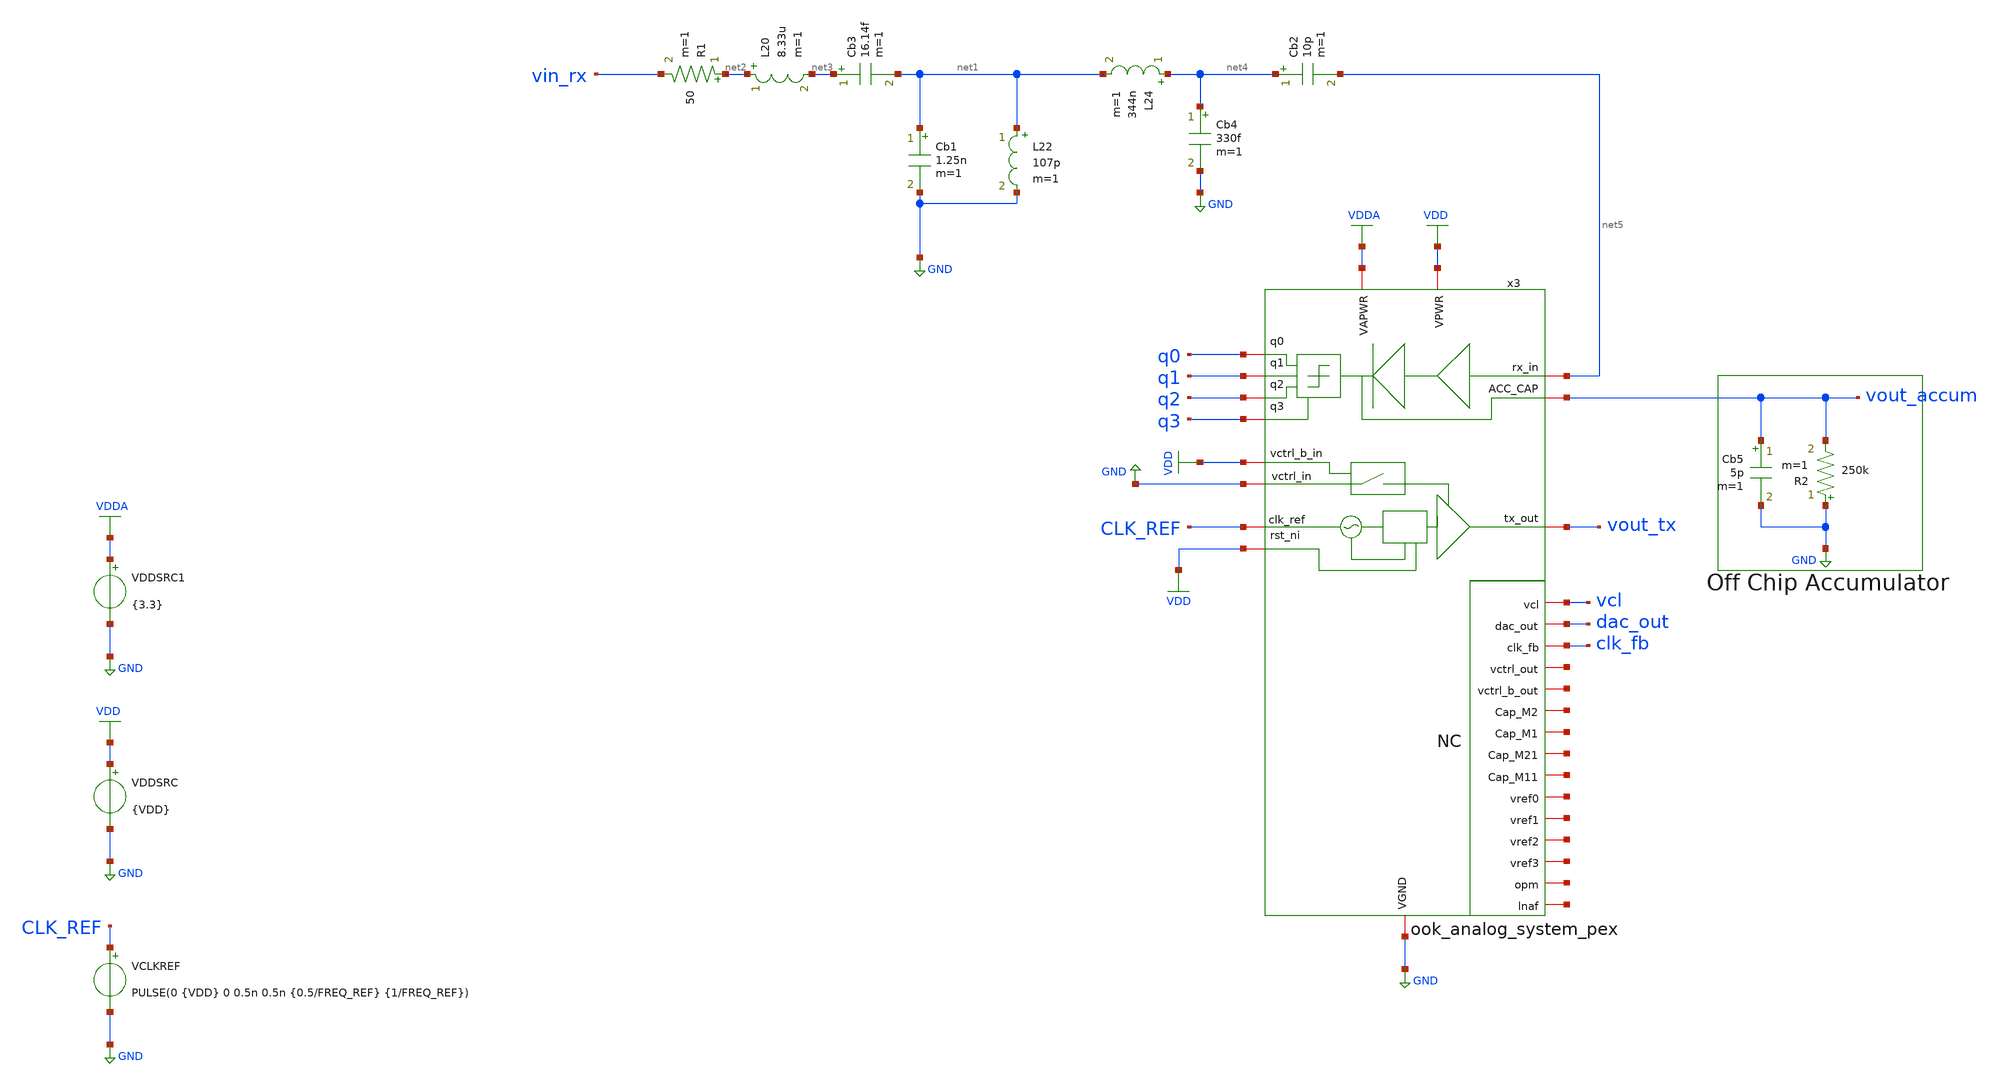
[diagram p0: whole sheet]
** sch_path: macros/heichips26_ook_top/macros/ook_analog_system/testbenches/xschem/ook_analog_system_tb_tran.sch
**.subckt ook_analog_system_tb_tran
VCLKREF CLK_REF GND PULSE(0 {VDD} 0 0.5n 0.5n {0.5/FREQ_REF} {1/FREQ_REF})
VDDSRC VDD GND {VDD}
x3 VDDA vcl VDD q3 q2 vout_tx net5 q1 q0 GND net6 VDD net7 vout_accum net8 net9 net10 net11 net12
+ CLK_REF net13 clk_fb VDD dac_out GND net14 net15 net16 net17 ook_analog_system_pex
VDDSRC1 VDDA GND {3.3}
Cb5 vout_accum GND 5p m=1
R2 GND vout_accum 250k m=1
Cb2 net4 net5 10p m=1
L20 net2 net3 8.33u m=1
R1 net2 vin_rx 50 m=1
Cb1 net1 GND 1.25n m=1
Cb3 net3 net1 16.14f m=1
L22 net1 GND 107p m=1
L24 net4 net1 344n m=1
Cb4 net4 GND 330f m=1
**** begin user architecture code


.param VDD=1.5
.param FREQ_REF=80e6
.param FREQ_FB=600e6
.options klu reltol=1e-3 abstol=1e-12 vntol=1e-6 gmin=1e-9 rshunt=1e12
.param b0=1 b1=0 b2=1 b3=0 b4=0 b5=1 b6=0 b7=1
.param bitsum={b0+b1+b2+b3+b4+b5+b6+b7}
.param parity={bitsum-2*int(bitsum/2)}

Vcarrier ncar 0 SINE(0 1m 433.92e6)

Bvenv nenv 0 V =  (time<10e-6)  ? 1 :  (time<15e-6)  ? (1-b0) : (time<20e-6) ? b0 :  (time<25e-6)  ?
+ (1-b1) : (time<30e-6) ? b1 :  (time<35e-6)  ? (1-b2) : (time<40e-6) ? b2 :  (time<45e-6)  ? (1-b3) :
+ (time<50e-6) ? b3 :  (time<55e-6)  ? (1-b4) : (time<60e-6) ? b4 :  (time<65e-6)  ? (1-b5) : (time<70e-6) ? b5 :
+  (time<75e-6)  ? (1-b6) : (time<80e-6) ? b6 :  (time<85e-6)  ? (1-b7) : (time<90e-6) ? b7 :  (time<100e-6) ?
+ parity :  1

Bvin1 vin_rx 0 V={(V(nenv)*V(ncar))}
.save vout_tx clk_fb vcl q0 q1 q2 q3 vout_accum vin_rx
.tran 100p 150u 0 100p



.lib cornerMOSlv.lib mos_tt
.lib cornerMOShv.lib mos_tt
.lib cornerRES.lib res_typ
.lib cornerDIO.lib dio_tt
.lib cornerCAP.lib cap_typ
.include /home/belal/HeiChips/heichips26-on-off/macros/heichips26_ook_top/macros/dac/netlist/xspice/dac.xspice
.include /home/belal/HeiChips/heichips26-on-off/macros/heichips26_ook_top/macros/ook_analog_system/netlist/pex/ook_transmitter_magic_pex_3.spice
.include /home/belal/HeiChips/heichips26-on-off/macros/heichips26_ook_top/macros/ook_analog_system/netlist/pex/ook_analog_system_magic_pex_3.spice
.include /home/belal/HeiChips/heichips26-on-off/IHP-Open-PDK/ihp-sg13cmos5l/libs.tech/ngspice/models/cap_mfringe.lib
.include /home/belal/HeiChips/heichips26-on-off/macros/heichips26_ook_top/macros/ook_analog_system/netlist/pex/vco_magic_pex_3.spice
.include /home/belal/HeiChips/heichips26-on-off/macros/heichips26_ook_top/macros/ook_analog_system/netlist/pex/output_buffer_magic_pex_3.spice

**** end user architecture code
**.ends
.GLOBAL GND
.GLOBAL VDD
.GLOBAL VDDA
.end
